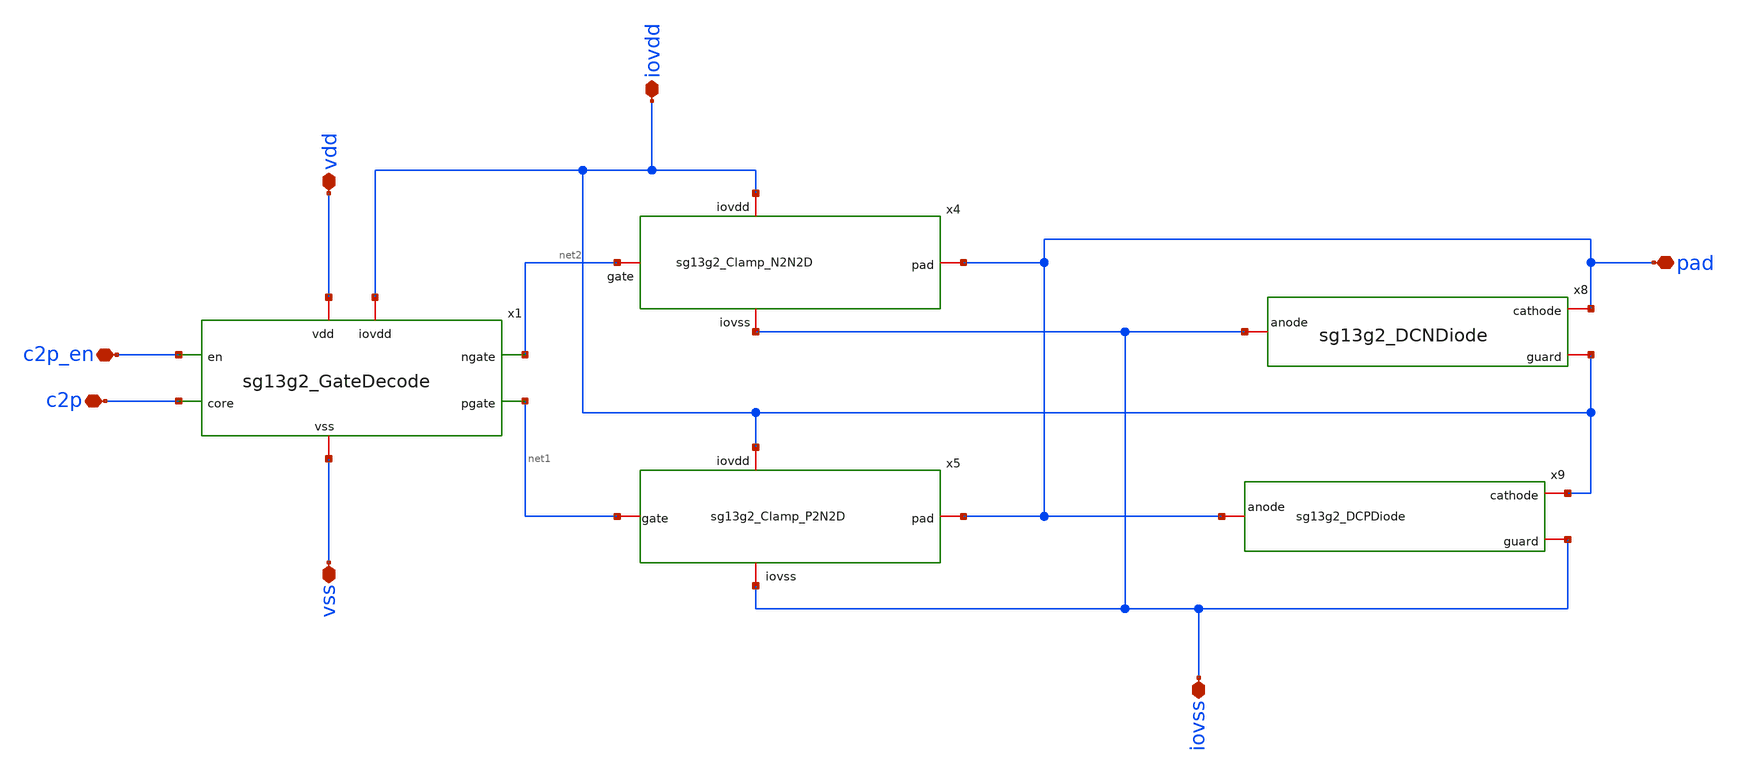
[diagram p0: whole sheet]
** sch_path: CDR4176-main/schematic/xschem/project_io/sg13g2_IOPadTriOut4mA/sg13g2_IOPadTriOut4mA.sch
**.subckt sg13g2_IOPadTriOut4mA iovss pad vss c2p vdd iovdd c2p_en
*.iopin iovss
*.iopin pad
*.iopin vss
*.iopin c2p
*.iopin vdd
*.iopin iovdd
*.iopin c2p_en
x8 pad iovss iovdd sg13g2_DCNDiode
x9 iovdd pad iovss sg13g2_DCPDiode
x4 iovdd pad net2 iovss sg13g2_Clamp_N2N2D
x5 iovdd net1 iovss pad sg13g2_Clamp_P2N2D
x1 vdd iovdd c2p_en net2 net1 c2p vss sg13g2_GateDecode
**.ends
.end
